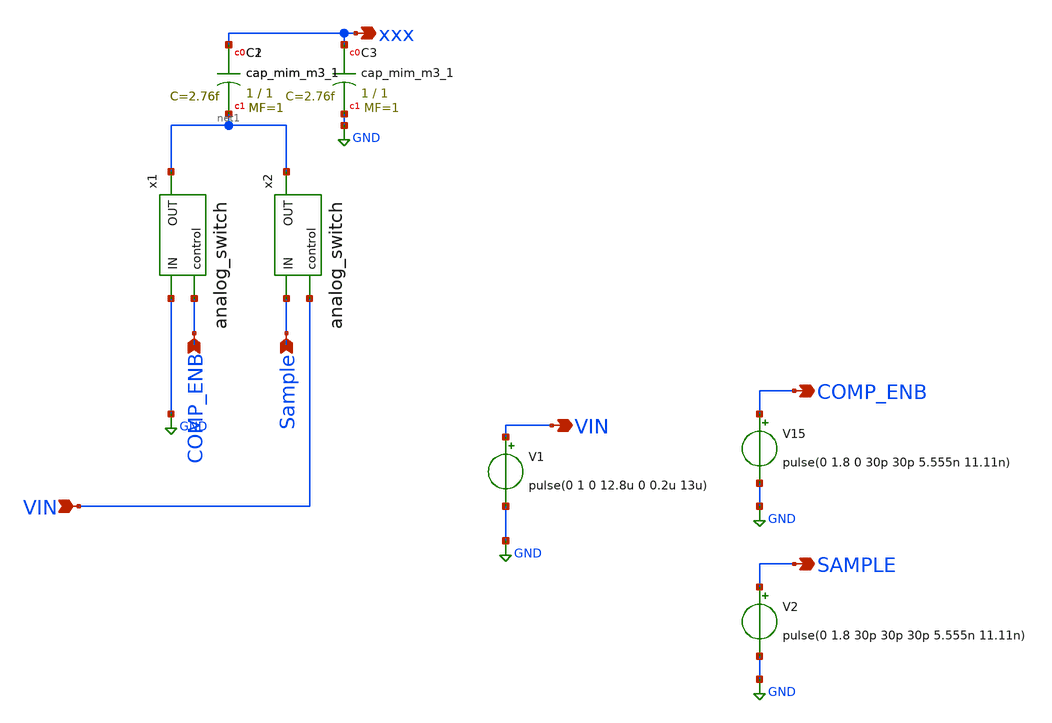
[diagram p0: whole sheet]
** sch_path: tb1.sch
* Copyright 2021 Stefan Frederik Schippers
* Licensed under the Apache License, Version 2.0 (the "License");
* you may not use this file except in compliance with the License.
* You may obtain a copy of the License at
* https://www.apache.org/licenses/LICENSE-2.0
* Unless required by applicable law or agreed to in writing, software
* distributed under the License is distributed on an "AS IS" BASIS,
* WITHOUT WARRANTIES OR CONDITIONS OF ANY KIND, either express or implied.
* See the License for the specific language governing permissions and
* limitations under the License.
**.subckt tb1 xxx VIN COMP_ENB Sample VIN COMP_ENB SAMPLE
*.opin xxx
*.ipin VIN
*.ipin COMP_ENB
*.ipin Sample
*.opin VIN
*.opin COMP_ENB
*.opin SAMPLE
x1 COMP_ENB net1 GND analog_switch
x2 VIN net1 Sample analog_switch
V1 VIN GND pulse(0 1 0 12.8u 0 0.2u 13u)
V15 COMP_ENB GND pulse(0 1.8 0 30p 30p 5.555n 11.11n)
V2 SAMPLE GND pulse(0 1.8 30p 30p 30p 5.555n 11.11n)
XC1 xxx net1 sky130_fd_pr__cap_mim_m3_1 W=1 L=1 MF=1 m=1
XC2 xxx net1 sky130_fd_pr__cap_mim_m3_1 W=1 L=1 MF=1 m=1
XC3 xxx GND sky130_fd_pr__cap_mim_m3_1 W=1 L=1 MF=1 m=1
**** begin user architecture code
 .lib $::SKYWATER_MODELS/sky130.lib.spice tt
.include $::SKYWATER_STDCELLS/sky130_fd_sc_hd.spice



.options acct list
.temp 25
.control
tran 100n 13u
write tb_saradc.raw
.endc


**** end user architecture code
**.ends
.GLOBAL GND
.end
